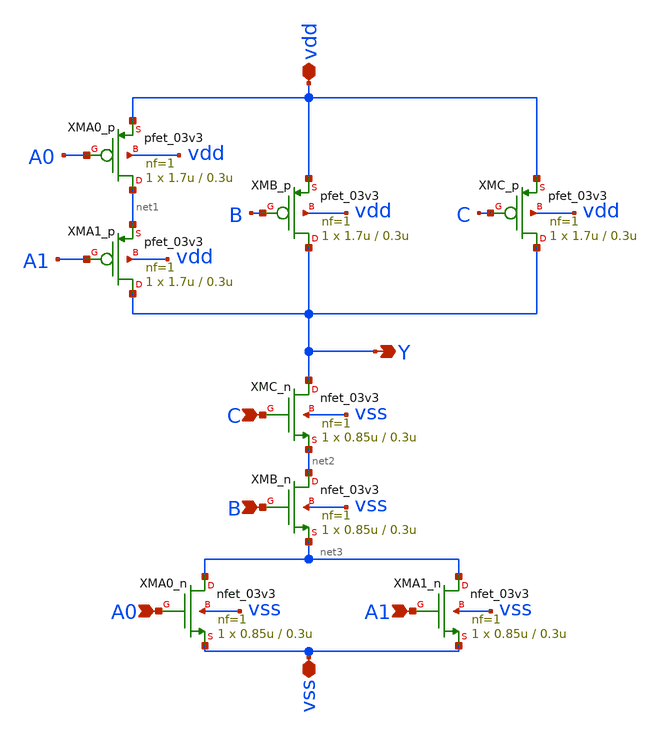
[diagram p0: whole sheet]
** sch_path: gf180mcu_osu_sc_gp9t3v3/xschem/gf180mcu_osu_sc_gp9t3v3__oai211_1.sch
**.subckt gf180mcu_osu_sc_gp9t3v3__oai211_1 vdd vss Y A0 A1 B C
*.iopin vdd
*.iopin vss
*.opin Y
*.ipin A0
*.ipin A1
*.ipin B
*.ipin C
XMA0_p net1 A0 vdd vdd pfet_03v3 L=0.3u W=1.7u nf=1 ad='int((nf+1)/2) * W/nf * 0.18u' as='int((nf+2)/2) * W/nf * 0.18u'
+ pd='2*int((nf+1)/2) * (W/nf + 0.18u)' ps='2*int((nf+2)/2) * (W/nf + 0.18u)' nrd='0.18u / W' nrs='0.18u / W'
+ sa=0 sb=0 sd=0 m=1
XMA0_n net3 A0 vss vss nfet_03v3 L=0.3u W=0.85u nf=1 ad='int((nf+1)/2) * W/nf * 0.18u' as='int((nf+2)/2) * W/nf * 0.18u'
+ pd='2*int((nf+1)/2) * (W/nf + 0.18u)' ps='2*int((nf+2)/2) * (W/nf + 0.18u)' nrd='0.18u / W' nrs='0.18u / W'
+ sa=0 sb=0 sd=0 m=1
XMA1_n net3 A1 vss vss nfet_03v3 L=0.3u W=0.85u nf=1 ad='int((nf+1)/2) * W/nf * 0.18u' as='int((nf+2)/2) * W/nf * 0.18u'
+ pd='2*int((nf+1)/2) * (W/nf + 0.18u)' ps='2*int((nf+2)/2) * (W/nf + 0.18u)' nrd='0.18u / W' nrs='0.18u / W'
+ sa=0 sb=0 sd=0 m=1
XMB_n net2 B net3 vss nfet_03v3 L=0.3u W=0.85u nf=1 ad='int((nf+1)/2) * W/nf * 0.18u' as='int((nf+2)/2) * W/nf * 0.18u'
+ pd='2*int((nf+1)/2) * (W/nf + 0.18u)' ps='2*int((nf+2)/2) * (W/nf + 0.18u)' nrd='0.18u / W' nrs='0.18u / W'
+ sa=0 sb=0 sd=0 m=1
XMC_n Y C net2 vss nfet_03v3 L=0.3u W=0.85u nf=1 ad='int((nf+1)/2) * W/nf * 0.18u' as='int((nf+2)/2) * W/nf * 0.18u'
+ pd='2*int((nf+1)/2) * (W/nf + 0.18u)' ps='2*int((nf+2)/2) * (W/nf + 0.18u)' nrd='0.18u / W' nrs='0.18u / W'
+ sa=0 sb=0 sd=0 m=1
XMA1_p Y A1 net1 vdd pfet_03v3 L=0.3u W=1.7u nf=1 ad='int((nf+1)/2) * W/nf * 0.18u' as='int((nf+2)/2) * W/nf * 0.18u'
+ pd='2*int((nf+1)/2) * (W/nf + 0.18u)' ps='2*int((nf+2)/2) * (W/nf + 0.18u)' nrd='0.18u / W' nrs='0.18u / W'
+ sa=0 sb=0 sd=0 m=1
XMB_p Y B vdd vdd pfet_03v3 L=0.3u W=1.7u nf=1 ad='int((nf+1)/2) * W/nf * 0.18u' as='int((nf+2)/2) * W/nf * 0.18u'
+ pd='2*int((nf+1)/2) * (W/nf + 0.18u)' ps='2*int((nf+2)/2) * (W/nf + 0.18u)' nrd='0.18u / W' nrs='0.18u / W'
+ sa=0 sb=0 sd=0 m=1
XMC_p Y C vdd vdd pfet_03v3 L=0.3u W=1.7u nf=1 ad='int((nf+1)/2) * W/nf * 0.18u' as='int((nf+2)/2) * W/nf * 0.18u'
+ pd='2*int((nf+1)/2) * (W/nf + 0.18u)' ps='2*int((nf+2)/2) * (W/nf + 0.18u)' nrd='0.18u / W' nrs='0.18u / W'
+ sa=0 sb=0 sd=0 m=1
**.ends
.end
